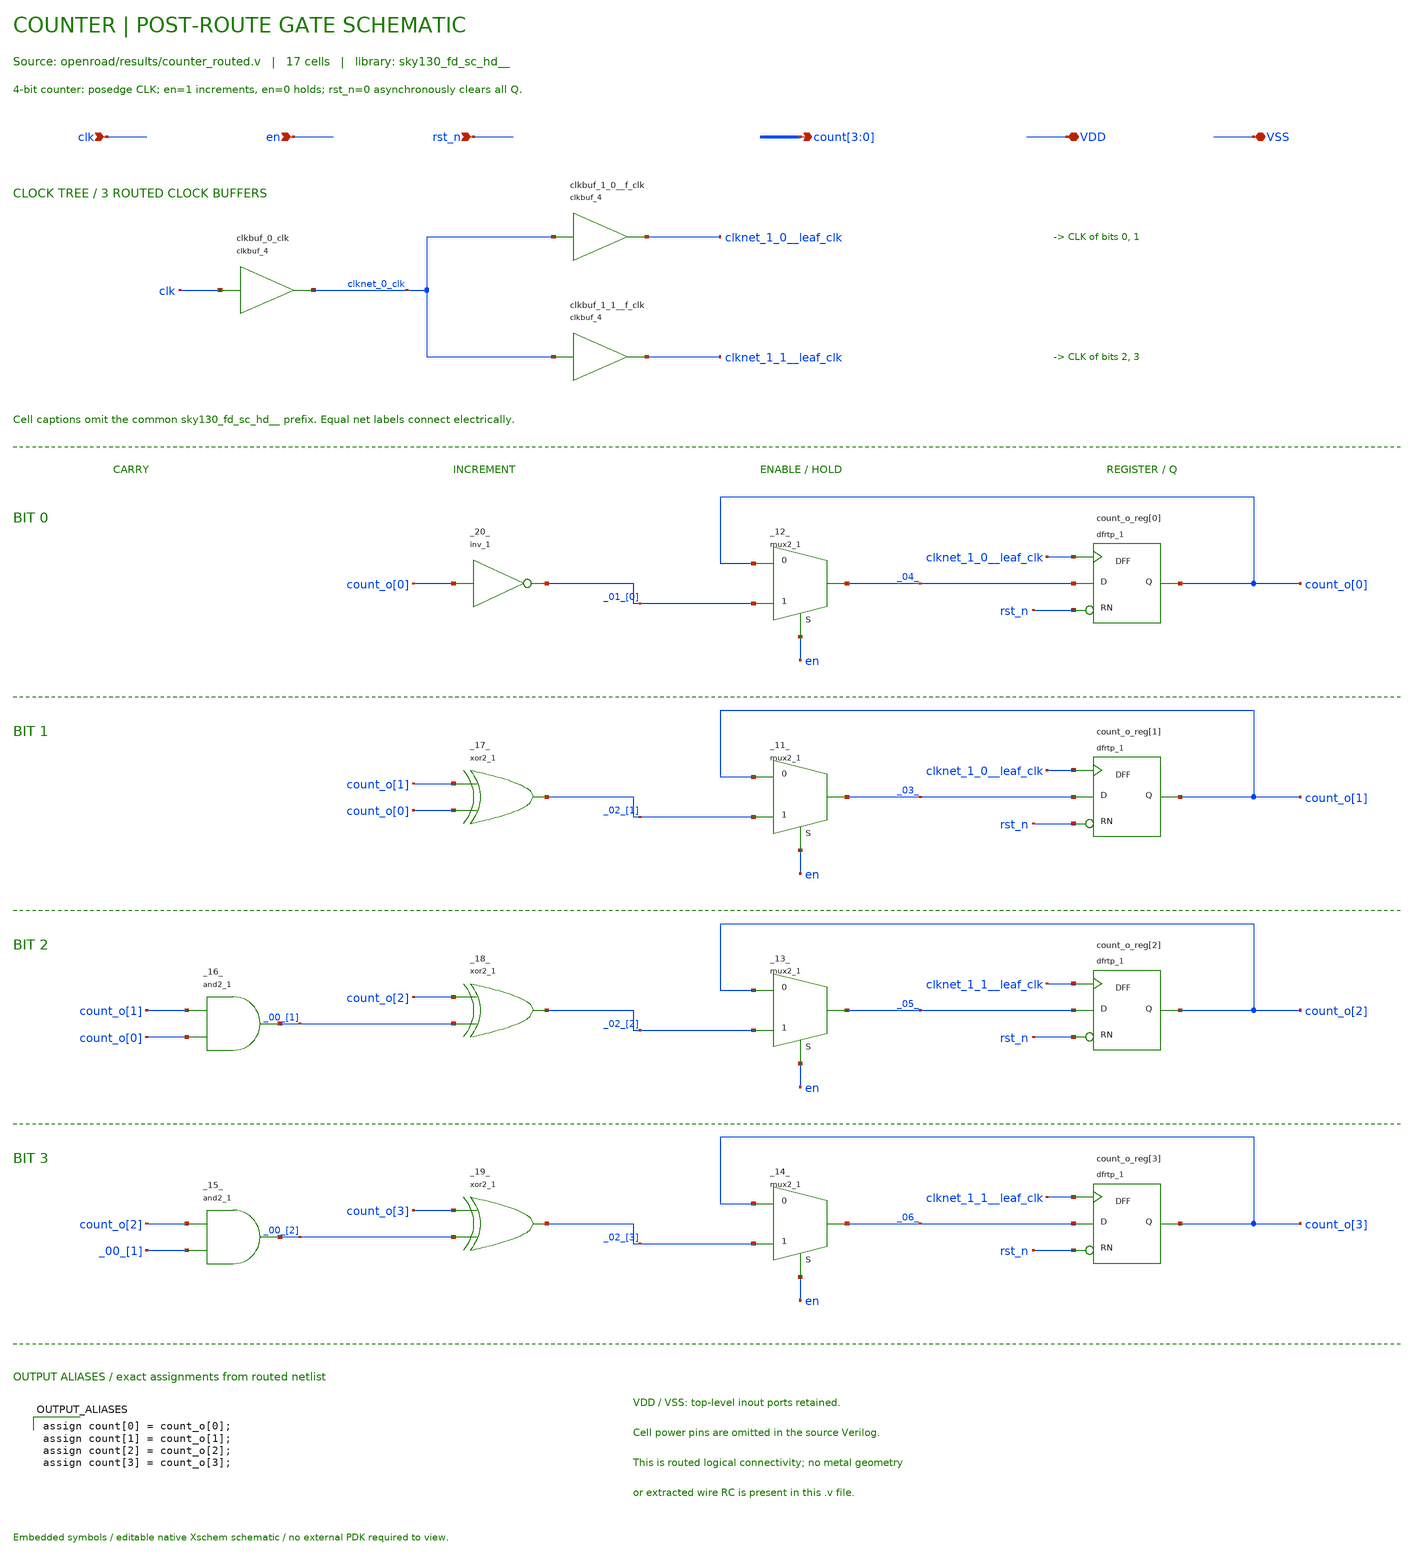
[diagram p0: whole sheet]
** sch_path: examples/counter/counter_dff/counter_routed.sch
* Copyright (C) 1998-2026 Stefan Frederik Schippers
* This program is free software; you can redistribute it and/or modify
* it under the terms of the GNU General Public License as published by
* the Free Software Foundation; either version 2 of the License, or
* (at your option) any later version.
**.subckt counter_routed clk en rst_n count[3],count[2],count[1],count[0] VDD VSS
*.ipin clk
*.ipin en
*.ipin rst_n
*.opin count[3],count[2],count[1],count[0]
*.iopin VDD
*.iopin VSS
**** begin user architecture code

assign count[0] = count_o[0];
assign count[1] = count_o[1];
assign count[2] = count_o[2];
assign count[3] = count_o[3];

**** end user architecture code
**.ends
.end
